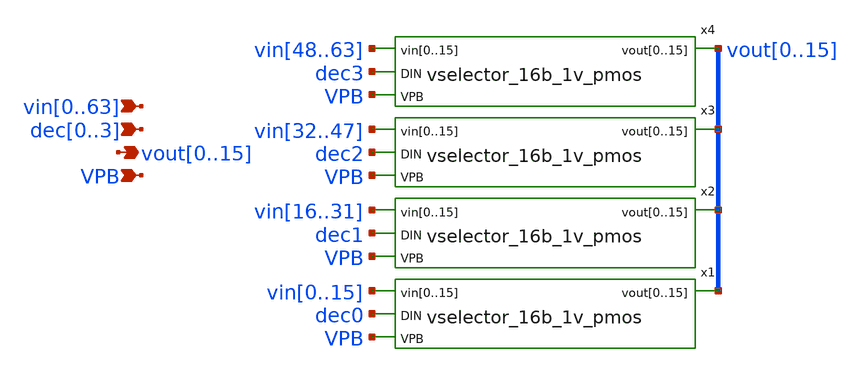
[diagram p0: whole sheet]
** sch_path: xschem/vselector_6b_1v_stage_1_pmos.sch
**.subckt vselector_6b_1v_stage_1_pmos
*+ vin0,vin1,vin2,vin3,vin4,vin5,vin6,vin7,vin8,vin9,vin10,vin11,vin12,vin13,vin14,vin15,vin16,vin17,vin18,vin19,vin20,vin21,vin22,vin23,vin24,vin25,vin26,vin27,vin28,vin29,vin30,vin31,vin32,vin33,vin34,vin35,vin36,vin37,vin38,vin39,vin40,vin41,vin42,vin43,vin44,vin45,vin46,vin47,vin48,vin49,vin50,vin51,vin52,vin53,vin54,vin55,vin56,vin57,vin58,vin59,vin60,vin61,vin62,vin63
*+ vout0,vout1,vout2,vout3,vout4,vout5,vout6,vout7,vout8,vout9,vout10,vout11,vout12,vout13,vout14,vout15 VPB dec0,dec1,dec2,dec3
*.ipin
*+ vin0,vin1,vin2,vin3,vin4,vin5,vin6,vin7,vin8,vin9,vin10,vin11,vin12,vin13,vin14,vin15,vin16,vin17,vin18,vin19,vin20,vin21,vin22,vin23,vin24,vin25,vin26,vin27,vin28,vin29,vin30,vin31,vin32,vin33,vin34,vin35,vin36,vin37,vin38,vin39,vin40,vin41,vin42,vin43,vin44,vin45,vin46,vin47,vin48,vin49,vin50,vin51,vin52,vin53,vin54,vin55,vin56,vin57,vin58,vin59,vin60,vin61,vin62,vin63
*.opin
*+ vout0,vout1,vout2,vout3,vout4,vout5,vout6,vout7,vout8,vout9,vout10,vout11,vout12,vout13,vout14,vout15
*.ipin VPB
*.ipin dec0,dec1,dec2,dec3
x1 vin0 vin1 vin2 vin3 vin4 vin5 vin6 vin7 vin8 vin9 vin10 vin11 vin12 vin13 vin14 vin15 dec0 vout0
+ vout1 vout2 vout3 vout4 vout5 vout6 vout7 vout8 vout9 vout10 vout11 vout12 vout13 vout14 vout15 VPB
+ vselector_16b_1v_pmos
x2 vin16 vin17 vin18 vin19 vin20 vin21 vin22 vin23 vin24 vin25 vin26 vin27 vin28 vin29 vin30 vin31
+ dec1 vout0 vout1 vout2 vout3 vout4 vout5 vout6 vout7 vout8 vout9 vout10 vout11 vout12 vout13 vout14
+ vout15 VPB vselector_16b_1v_pmos
x3 vin32 vin33 vin34 vin35 vin36 vin37 vin38 vin39 vin40 vin41 vin42 vin43 vin44 vin45 vin46 vin47
+ dec2 vout0 vout1 vout2 vout3 vout4 vout5 vout6 vout7 vout8 vout9 vout10 vout11 vout12 vout13 vout14
+ vout15 VPB vselector_16b_1v_pmos
x4 vin48 vin49 vin50 vin51 vin52 vin53 vin54 vin55 vin56 vin57 vin58 vin59 vin60 vin61 vin62 vin63
+ dec3 vout0 vout1 vout2 vout3 vout4 vout5 vout6 vout7 vout8 vout9 vout10 vout11 vout12 vout13 vout14
+ vout15 VPB vselector_16b_1v_pmos
**.ends

* expanding   symbol:  vselector_16b_1v_pmos.sym # of pins=4
** sym_path: xschem/vselector_16b_1v_pmos.sym
** sch_path: xschem/vselector_16b_1v_pmos.sch
.subckt vselector_16b_1v_pmos vin0 vin1 vin2 vin3 vin4 vin5 vin6 vin7 vin8 vin9 vin10 vin11 vin12
+ vin13 vin14 vin15 DIN vout0 vout1 vout2 vout3 vout4 vout5 vout6 vout7 vout8 vout9 vout10 vout11 vout12
+ vout13 vout14 vout15 VPB
*.ipin vin0,vin1,vin2,vin3,vin4,vin5,vin6,vin7,vin8,vin9,vin10,vin11,vin12,vin13,vin14,vin15
*.opin
*+ vout0,vout1,vout2,vout3,vout4,vout5,vout6,vout7,vout8,vout9,vout10,vout11,vout12,vout13,vout14,vout15
*.ipin VPB
*.ipin DIN
.param wp=0.42 wn=0.42 l=0.5

XM1 vout0 DIN vin0 VPB sky130_fd_pr__pfet_g5v0d10v5 L=l W=wp nf=1 ad='int((nf+1)/2) * W/nf * 0.29' as='int((nf+2)/2) * W/nf * 0.29'
+ pd='2*int((nf+1)/2) * (W/nf + 0.29)' ps='2*int((nf+2)/2) * (W/nf + 0.29)' nrd='0.29 / W' nrs='0.29 / W'
+ sa=0 sb=0 sd=0 mult=1 m=1
XM2 vout1 DIN vin1 VPB sky130_fd_pr__pfet_g5v0d10v5 L=l W=wp nf=1 ad='int((nf+1)/2) * W/nf * 0.29' as='int((nf+2)/2) * W/nf * 0.29'
+ pd='2*int((nf+1)/2) * (W/nf + 0.29)' ps='2*int((nf+2)/2) * (W/nf + 0.29)' nrd='0.29 / W' nrs='0.29 / W'
+ sa=0 sb=0 sd=0 mult=1 m=1
XM3 vout2 DIN vin2 VPB sky130_fd_pr__pfet_g5v0d10v5 L=l W=wp nf=1 ad='int((nf+1)/2) * W/nf * 0.29' as='int((nf+2)/2) * W/nf * 0.29'
+ pd='2*int((nf+1)/2) * (W/nf + 0.29)' ps='2*int((nf+2)/2) * (W/nf + 0.29)' nrd='0.29 / W' nrs='0.29 / W'
+ sa=0 sb=0 sd=0 mult=1 m=1
XM4 vout3 DIN vin3 VPB sky130_fd_pr__pfet_g5v0d10v5 L=l W=wp nf=1 ad='int((nf+1)/2) * W/nf * 0.29' as='int((nf+2)/2) * W/nf * 0.29'
+ pd='2*int((nf+1)/2) * (W/nf + 0.29)' ps='2*int((nf+2)/2) * (W/nf + 0.29)' nrd='0.29 / W' nrs='0.29 / W'
+ sa=0 sb=0 sd=0 mult=1 m=1
XM5 vout4 DIN vin4 VPB sky130_fd_pr__pfet_g5v0d10v5 L=l W=wp nf=1 ad='int((nf+1)/2) * W/nf * 0.29' as='int((nf+2)/2) * W/nf * 0.29'
+ pd='2*int((nf+1)/2) * (W/nf + 0.29)' ps='2*int((nf+2)/2) * (W/nf + 0.29)' nrd='0.29 / W' nrs='0.29 / W'
+ sa=0 sb=0 sd=0 mult=1 m=1
XM6 vout5 DIN vin5 VPB sky130_fd_pr__pfet_g5v0d10v5 L=l W=wp nf=1 ad='int((nf+1)/2) * W/nf * 0.29' as='int((nf+2)/2) * W/nf * 0.29'
+ pd='2*int((nf+1)/2) * (W/nf + 0.29)' ps='2*int((nf+2)/2) * (W/nf + 0.29)' nrd='0.29 / W' nrs='0.29 / W'
+ sa=0 sb=0 sd=0 mult=1 m=1
XM7 vout6 DIN vin6 VPB sky130_fd_pr__pfet_g5v0d10v5 L=l W=wp nf=1 ad='int((nf+1)/2) * W/nf * 0.29' as='int((nf+2)/2) * W/nf * 0.29'
+ pd='2*int((nf+1)/2) * (W/nf + 0.29)' ps='2*int((nf+2)/2) * (W/nf + 0.29)' nrd='0.29 / W' nrs='0.29 / W'
+ sa=0 sb=0 sd=0 mult=1 m=1
XM8 vout7 DIN vin7 VPB sky130_fd_pr__pfet_g5v0d10v5 L=l W=wp nf=1 ad='int((nf+1)/2) * W/nf * 0.29' as='int((nf+2)/2) * W/nf * 0.29'
+ pd='2*int((nf+1)/2) * (W/nf + 0.29)' ps='2*int((nf+2)/2) * (W/nf + 0.29)' nrd='0.29 / W' nrs='0.29 / W'
+ sa=0 sb=0 sd=0 mult=1 m=1
XM9 vout8 DIN vin8 VPB sky130_fd_pr__pfet_g5v0d10v5 L=l W=wp nf=1 ad='int((nf+1)/2) * W/nf * 0.29' as='int((nf+2)/2) * W/nf * 0.29'
+ pd='2*int((nf+1)/2) * (W/nf + 0.29)' ps='2*int((nf+2)/2) * (W/nf + 0.29)' nrd='0.29 / W' nrs='0.29 / W'
+ sa=0 sb=0 sd=0 mult=1 m=1
XM10 vout9 DIN vin9 VPB sky130_fd_pr__pfet_g5v0d10v5 L=l W=wp nf=1 ad='int((nf+1)/2) * W/nf * 0.29' as='int((nf+2)/2) * W/nf * 0.29'
+ pd='2*int((nf+1)/2) * (W/nf + 0.29)' ps='2*int((nf+2)/2) * (W/nf + 0.29)' nrd='0.29 / W' nrs='0.29 / W'
+ sa=0 sb=0 sd=0 mult=1 m=1
XM11 vout10 DIN vin10 VPB sky130_fd_pr__pfet_g5v0d10v5 L=l W=wp nf=1 ad='int((nf+1)/2) * W/nf * 0.29'
+ as='int((nf+2)/2) * W/nf * 0.29' pd='2*int((nf+1)/2) * (W/nf + 0.29)' ps='2*int((nf+2)/2) * (W/nf + 0.29)'
+ nrd='0.29 / W' nrs='0.29 / W' sa=0 sb=0 sd=0 mult=1 m=1
XM12 vout11 DIN vin11 VPB sky130_fd_pr__pfet_g5v0d10v5 L=l W=wp nf=1 ad='int((nf+1)/2) * W/nf * 0.29'
+ as='int((nf+2)/2) * W/nf * 0.29' pd='2*int((nf+1)/2) * (W/nf + 0.29)' ps='2*int((nf+2)/2) * (W/nf + 0.29)'
+ nrd='0.29 / W' nrs='0.29 / W' sa=0 sb=0 sd=0 mult=1 m=1
XM13 vout12 DIN vin12 VPB sky130_fd_pr__pfet_g5v0d10v5 L=l W=wp nf=1 ad='int((nf+1)/2) * W/nf * 0.29'
+ as='int((nf+2)/2) * W/nf * 0.29' pd='2*int((nf+1)/2) * (W/nf + 0.29)' ps='2*int((nf+2)/2) * (W/nf + 0.29)'
+ nrd='0.29 / W' nrs='0.29 / W' sa=0 sb=0 sd=0 mult=1 m=1
XM14 vout13 DIN vin13 VPB sky130_fd_pr__pfet_g5v0d10v5 L=l W=wp nf=1 ad='int((nf+1)/2) * W/nf * 0.29'
+ as='int((nf+2)/2) * W/nf * 0.29' pd='2*int((nf+1)/2) * (W/nf + 0.29)' ps='2*int((nf+2)/2) * (W/nf + 0.29)'
+ nrd='0.29 / W' nrs='0.29 / W' sa=0 sb=0 sd=0 mult=1 m=1
XM15 vout14 DIN vin14 VPB sky130_fd_pr__pfet_g5v0d10v5 L=l W=wp nf=1 ad='int((nf+1)/2) * W/nf * 0.29'
+ as='int((nf+2)/2) * W/nf * 0.29' pd='2*int((nf+1)/2) * (W/nf + 0.29)' ps='2*int((nf+2)/2) * (W/nf + 0.29)'
+ nrd='0.29 / W' nrs='0.29 / W' sa=0 sb=0 sd=0 mult=1 m=1
XM16 vout15 DIN vin15 VPB sky130_fd_pr__pfet_g5v0d10v5 L=l W=wp nf=1 ad='int((nf+1)/2) * W/nf * 0.29'
+ as='int((nf+2)/2) * W/nf * 0.29' pd='2*int((nf+1)/2) * (W/nf + 0.29)' ps='2*int((nf+2)/2) * (W/nf + 0.29)'
+ nrd='0.29 / W' nrs='0.29 / W' sa=0 sb=0 sd=0 mult=1 m=1
.ends

.end
